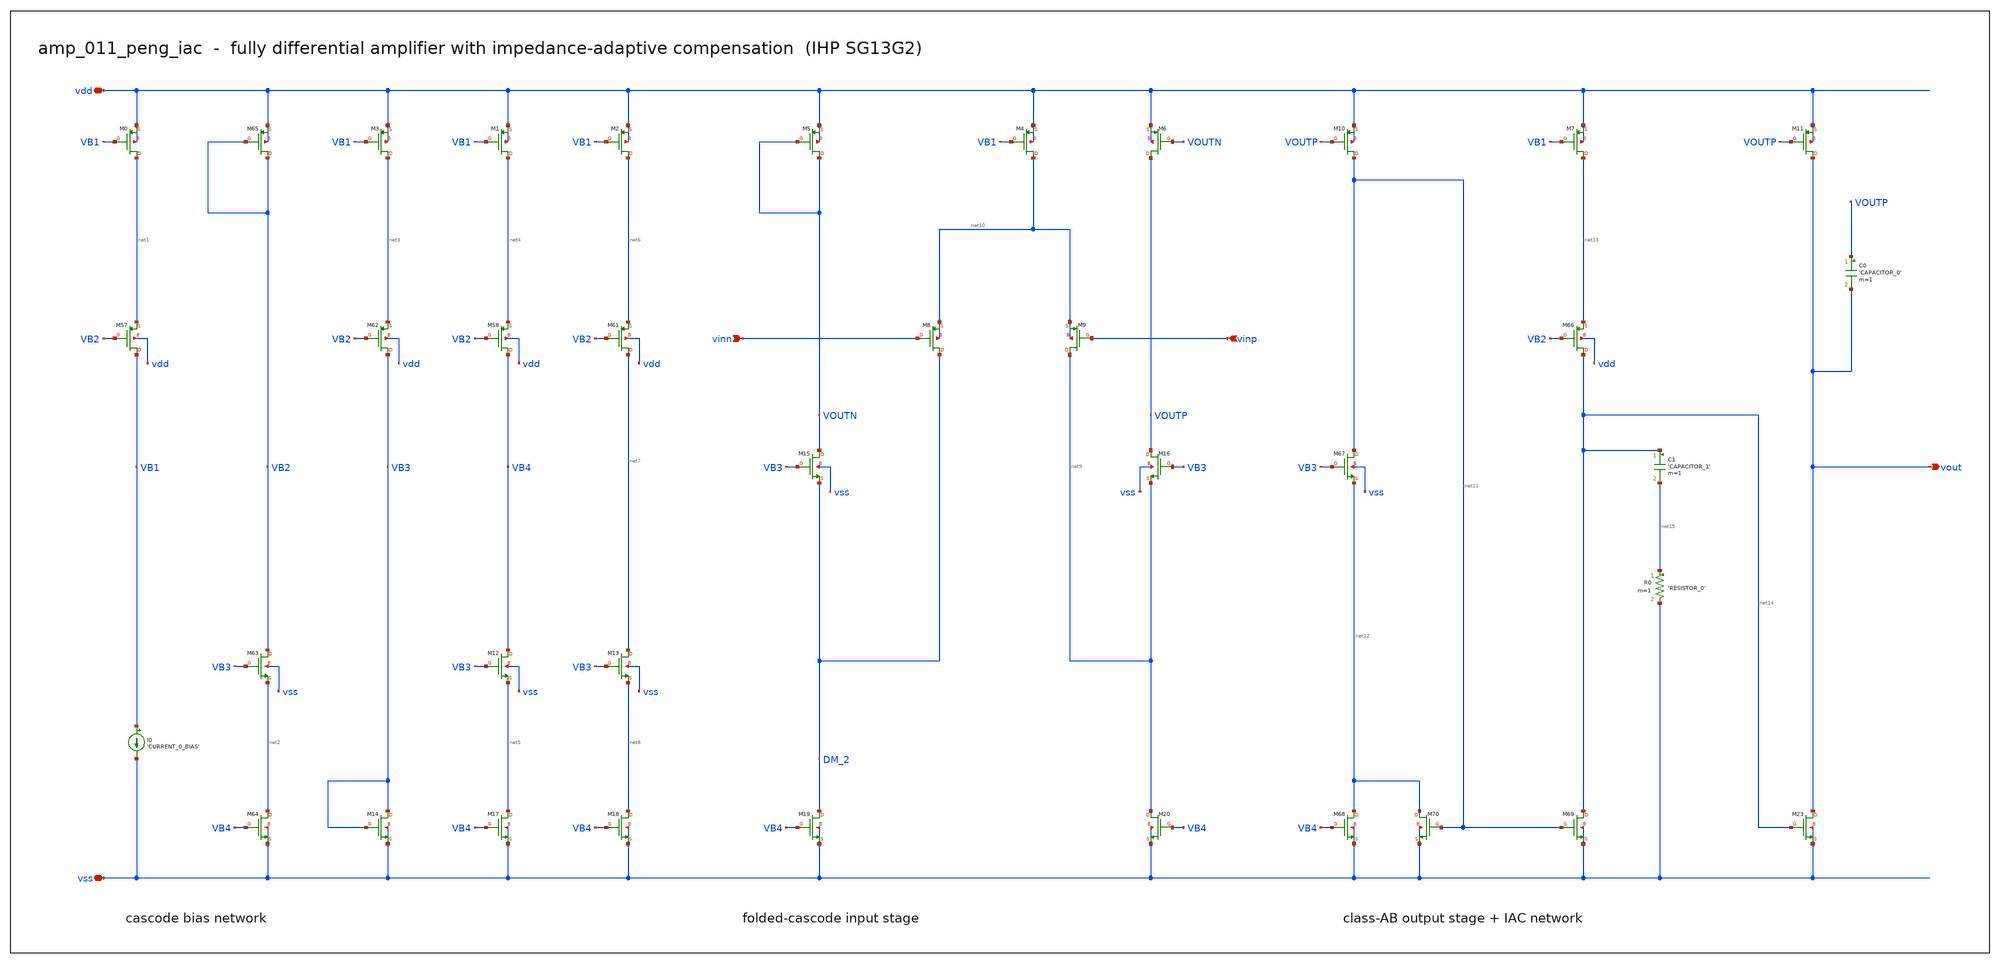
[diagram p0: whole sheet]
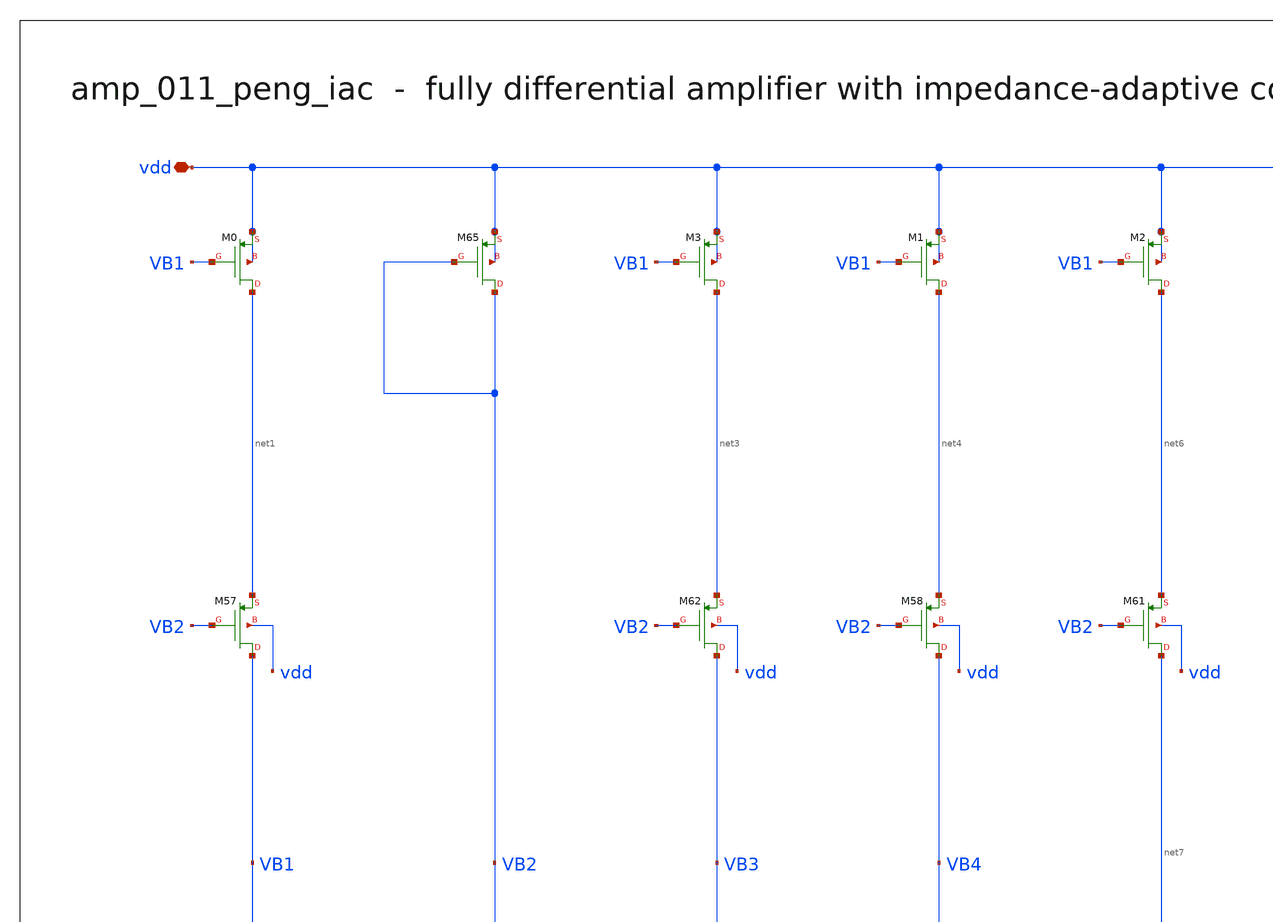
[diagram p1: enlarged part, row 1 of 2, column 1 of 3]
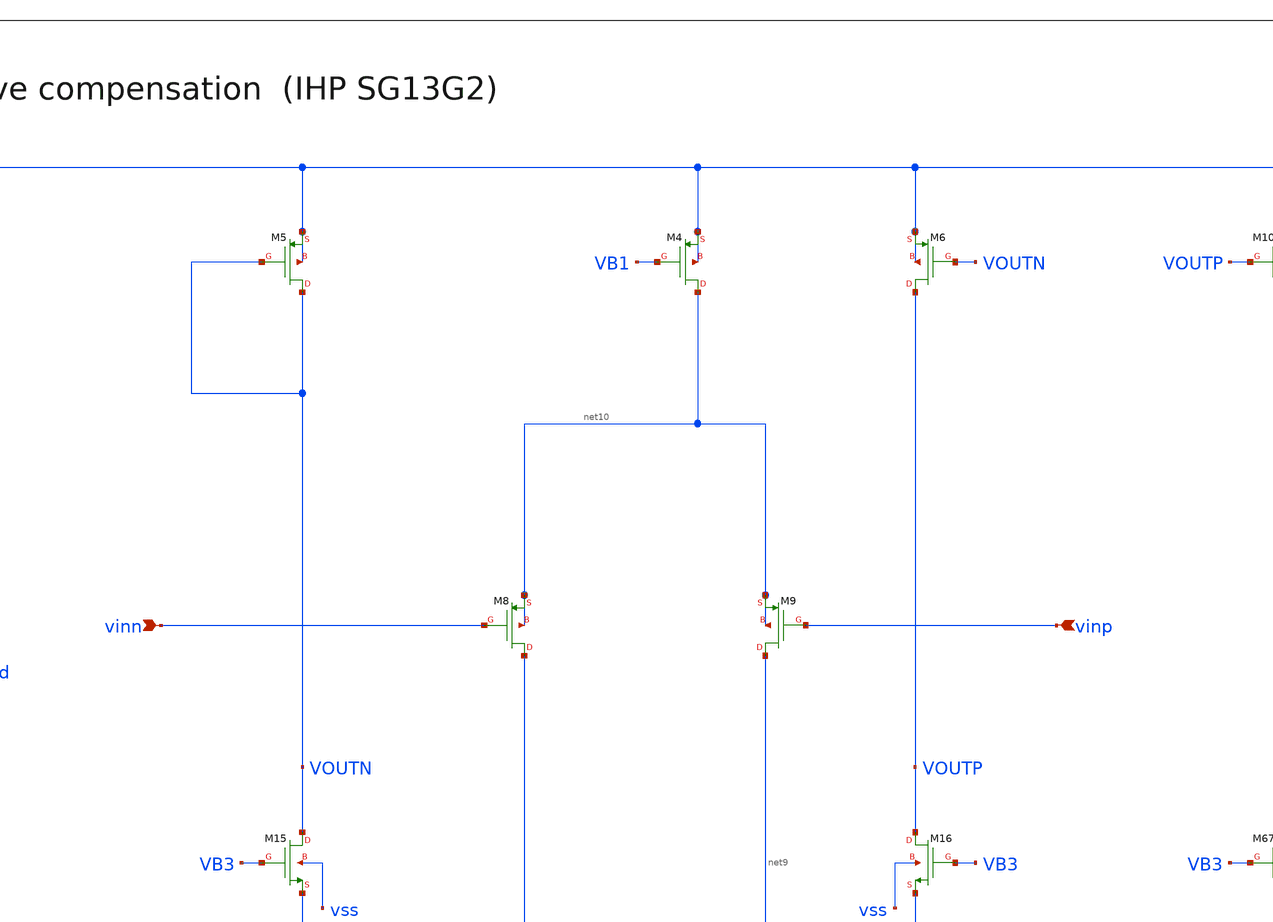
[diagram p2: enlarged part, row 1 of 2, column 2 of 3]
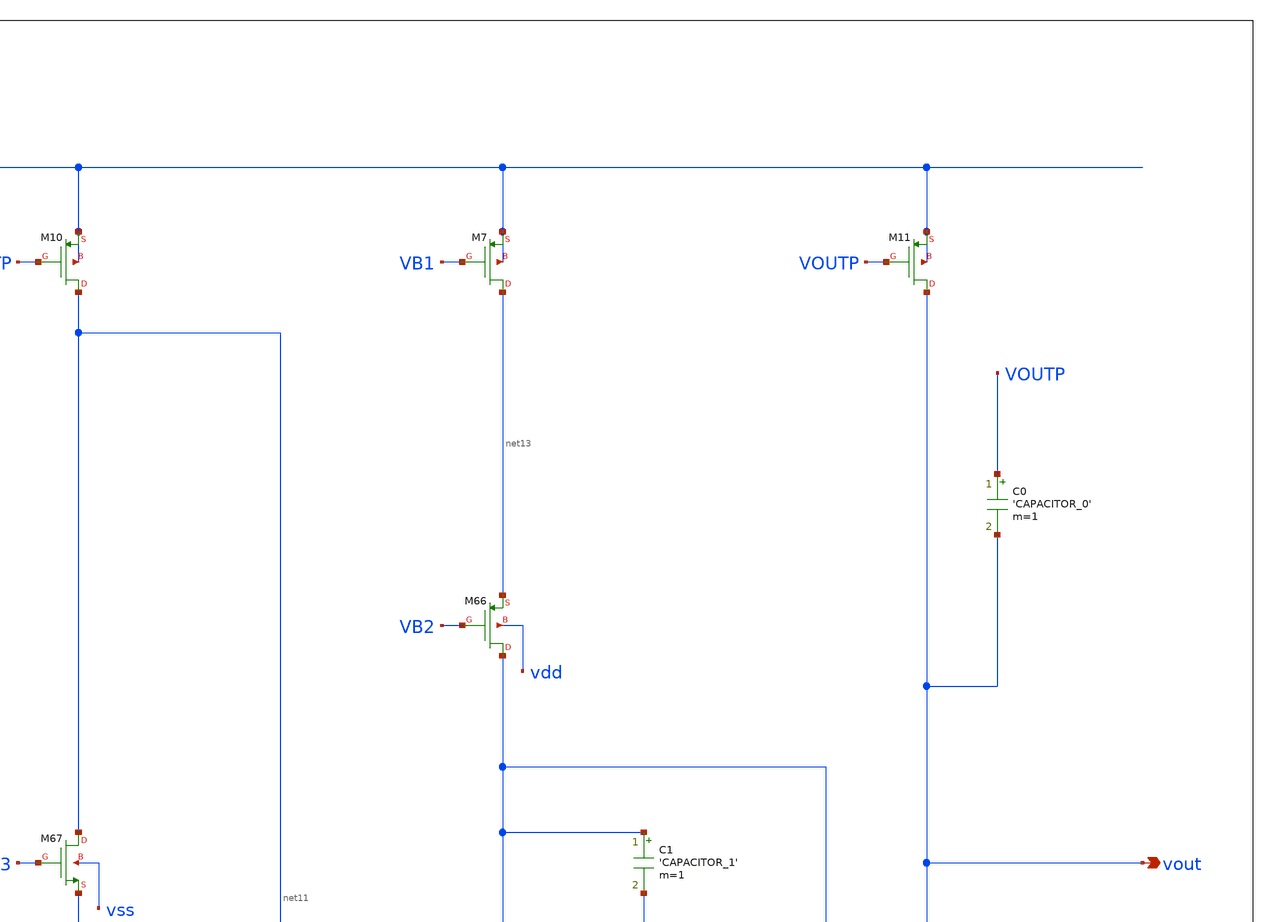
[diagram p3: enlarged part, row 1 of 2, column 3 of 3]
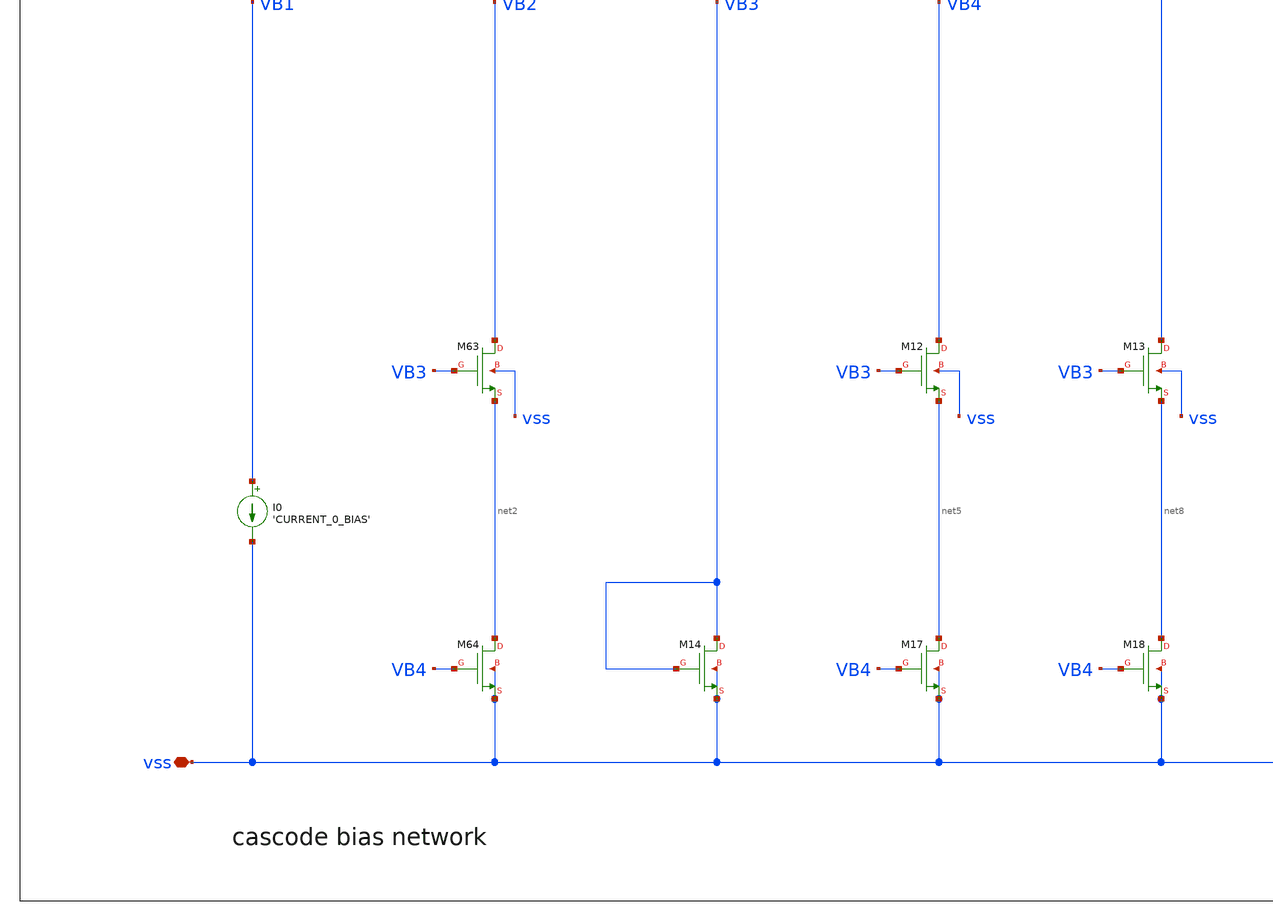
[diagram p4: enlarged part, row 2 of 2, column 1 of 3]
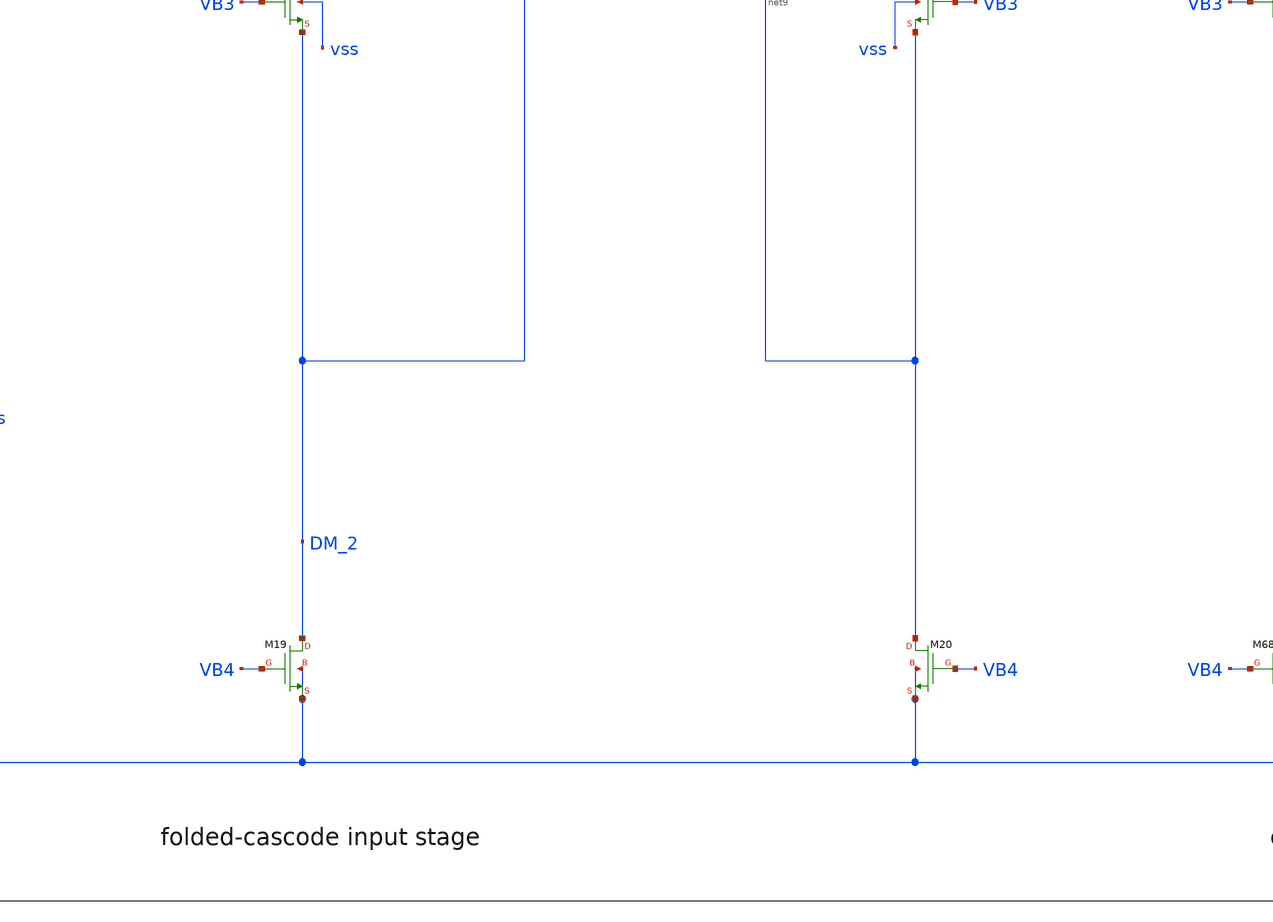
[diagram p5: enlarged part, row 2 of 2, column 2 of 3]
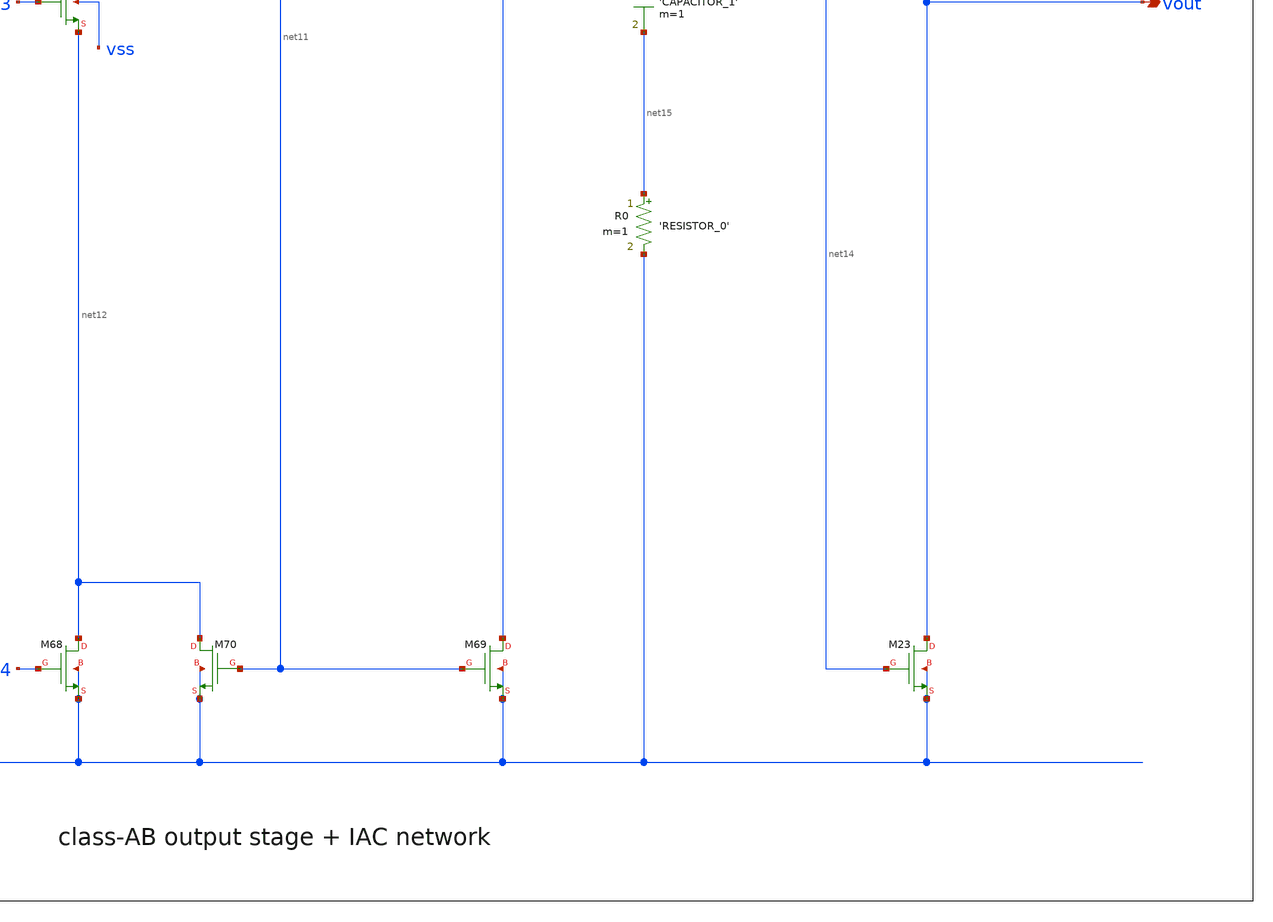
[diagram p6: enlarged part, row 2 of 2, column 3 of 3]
** sch_path: analog-db/drawings/publication/amp_011_peng_iac.sch
**.subckt amp_011_peng_iac vinn vinp vout vdd vss
*.ipin vinn
*.ipin vinp
*.opin vout
*.iopin vdd
*.iopin vss
XM0 net1 VB1 vdd vdd sg13_lv_pmos w=x_dut_xm0_w l=x_dut_xm0_l ng=1 m=x_dut_xm0_m
XM57 VB1 VB2 net1 vdd sg13_lv_pmos w=x_dut_xm57_w l=x_dut_xm57_l ng=1 m=x_dut_xm57_m
I0 VB1 vss 'CURRENT_0_BIAS'
XM65 VB2 VB2 vdd vdd sg13_lv_pmos w=x_dut_xm65_w l=x_dut_xm65_l ng=1 m=x_dut_xm65_m
XM63 VB2 VB3 net2 vss sg13_lv_nmos w=x_dut_xm63_w l=x_dut_xm63_l ng=1 m=x_dut_xm63_m
XM64 net2 VB4 vss vss sg13_lv_nmos w=x_dut_xm64_w l=x_dut_xm64_l ng=1 m=x_dut_xm64_m
XM3 net3 VB1 vdd vdd sg13_lv_pmos w=x_dut_xm3_w l=x_dut_xm3_l ng=1 m=x_dut_xm3_m
XM62 VB3 VB2 net3 vdd sg13_lv_pmos w=x_dut_xm62_w l=x_dut_xm62_l ng=1 m=x_dut_xm62_m
XM14 VB3 VB3 vss vss sg13_lv_nmos w=x_dut_xm14_w l=x_dut_xm14_l ng=1 m=x_dut_xm14_m
XM1 net4 VB1 vdd vdd sg13_lv_pmos w=x_dut_xm1_w l=x_dut_xm1_l ng=1 m=x_dut_xm1_m
XM58 VB4 VB2 net4 vdd sg13_lv_pmos w=x_dut_xm58_w l=x_dut_xm58_l ng=1 m=x_dut_xm58_m
XM12 VB4 VB3 net5 vss sg13_lv_nmos w=x_dut_xm12_w l=x_dut_xm12_l ng=1 m=x_dut_xm12_m
XM17 net5 VB4 vss vss sg13_lv_nmos w=x_dut_xm17_w l=x_dut_xm17_l ng=1 m=x_dut_xm17_m
XM2 net6 VB1 vdd vdd sg13_lv_pmos w=x_dut_xm2_w l=x_dut_xm2_l ng=1 m=x_dut_xm2_m
XM61 net7 VB2 net6 vdd sg13_lv_pmos w=x_dut_xm61_w l=x_dut_xm61_l ng=1 m=x_dut_xm61_m
XM13 net7 VB3 net8 vss sg13_lv_nmos w=x_dut_xm13_w l=x_dut_xm13_l ng=1 m=x_dut_xm13_m
XM18 net8 VB4 vss vss sg13_lv_nmos w=x_dut_xm18_w l=x_dut_xm18_l ng=1 m=x_dut_xm18_m
XM5 VOUTN VOUTN vdd vdd sg13_lv_pmos w=x_dut_xm5_w l=x_dut_xm5_l ng=1 m=x_dut_xm5_m
XM15 VOUTN VB3 DM_2 vss sg13_lv_nmos w=x_dut_xm15_w l=x_dut_xm15_l ng=1 m=x_dut_xm15_m
XM19 DM_2 VB4 vss vss sg13_lv_nmos w=x_dut_xm19_w l=x_dut_xm19_l ng=1 m=x_dut_xm19_m
XM6 VOUTP VOUTN vdd vdd sg13_lv_pmos w=x_dut_xm6_w l=x_dut_xm6_l ng=1 m=x_dut_xm6_m
XM16 VOUTP VB3 net9 vss sg13_lv_nmos w=x_dut_xm16_w l=x_dut_xm16_l ng=1 m=x_dut_xm16_m
XM20 net9 VB4 vss vss sg13_lv_nmos w=x_dut_xm20_w l=x_dut_xm20_l ng=1 m=x_dut_xm20_m
XM4 net10 VB1 vdd vdd sg13_lv_pmos w=x_dut_xm4_w l=x_dut_xm4_l ng=1 m=x_dut_xm4_m
XM8 DM_2 vinn net10 net10 sg13_lv_pmos w=x_dut_xm8_w l=x_dut_xm8_l ng=1 m=x_dut_xm8_m
XM9 net9 vinp net10 net10 sg13_lv_pmos w=x_dut_xm9_w l=x_dut_xm9_l ng=1 m=x_dut_xm9_m
XM10 net11 VOUTP vdd vdd sg13_lv_pmos w=x_dut_xm10_w l=x_dut_xm10_l ng=1 m=x_dut_xm10_m
XM67 net11 VB3 net12 vss sg13_lv_nmos w=x_dut_xm67_w l=x_dut_xm67_l ng=1 m=x_dut_xm67_m
XM68 net12 VB4 vss vss sg13_lv_nmos w=x_dut_xm68_w l=x_dut_xm68_l ng=1 m=x_dut_xm68_m
XM70 net12 net11 vss vss sg13_lv_nmos w=x_dut_xm70_w l=x_dut_xm70_l ng=1 m=x_dut_xm70_m
XM7 net13 VB1 vdd vdd sg13_lv_pmos w=x_dut_xm7_w l=x_dut_xm7_l ng=1 m=x_dut_xm7_m
XM66 net14 VB2 net13 vdd sg13_lv_pmos w=x_dut_xm66_w l=x_dut_xm66_l ng=1 m=x_dut_xm66_m
XM69 net14 net11 vss vss sg13_lv_nmos w=x_dut_xm69_w l=x_dut_xm69_l ng=1 m=x_dut_xm69_m
C1 net14 net15 'CAPACITOR_1' m=1
R0 net15 vss 'RESISTOR_0' m=1
XM11 vout VOUTP vdd vdd sg13_lv_pmos w=x_dut_xm11_w l=x_dut_xm11_l ng=1 m=x_dut_xm11_m
XM23 vout net14 vss vss sg13_lv_nmos w=x_dut_xm23_w l=x_dut_xm23_l ng=1 m=x_dut_xm23_m
C0 VOUTP vout 'CAPACITOR_0' m=1
**.ends
.end
